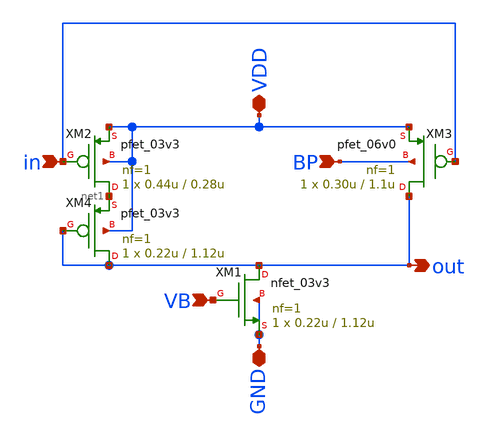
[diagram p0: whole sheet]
** sch_path: xschem_designs/STI_P.sch
**.subckt STI_P in out GND VDD BP VB
*.ipin in
*.opin out
*.iopin GND
*.iopin VDD
*.ipin BP
*.ipin VB
XM1 out VB GND GND nfet_03v3 L=1.12u W=0.22u nf=1 ad='int((nf+1)/2) * W/nf * 0.18u' as='int((nf+2)/2) * W/nf * 0.18u'
+ pd='2*int((nf+1)/2) * (W/nf + 0.18u)' ps='2*int((nf+2)/2) * (W/nf + 0.18u)' nrd='0.18u / W' nrs='0.18u / W'
+ sa=0 sb=0 sd=0 m=1 par=1
XM2 net1 in VDD VDD pfet_03v3 L=0.28u W=0.44u nf=1 ad='int((nf+1)/2) * W/nf * 0.18u' as='int((nf+2)/2) * W/nf * 0.18u'
+ pd='2*int((nf+1)/2) * (W/nf + 0.18u)' ps='2*int((nf+2)/2) * (W/nf + 0.18u)' nrd='0.18u / W' nrs='0.18u / W'
+ sa=0 sb=0 sd=0 m=1 par=1
XM3 out in VDD BP pfet_06v0 L=1.1u W=0.30u nf=1 ad='int((nf+1)/2) * W/nf * 0.18u' as='int((nf+2)/2) * W/nf * 0.18u'
+ pd='2*int((nf+1)/2) * (W/nf + 0.18u)' ps='2*int((nf+2)/2) * (W/nf + 0.18u)' nrd='0.18u / W' nrs='0.18u / W'
+ sa=0 sb=0 sd=0 m=1
XM4 out out net1 VDD pfet_03v3 L=1.12u W=0.22u nf=1 ad='int((nf+1)/2) * W/nf * 0.18u' as='int((nf+2)/2) * W/nf * 0.18u'
+ pd='2*int((nf+1)/2) * (W/nf + 0.18u)' ps='2*int((nf+2)/2) * (W/nf + 0.18u)' nrd='0.18u / W' nrs='0.18u / W'
+ sa=0 sb=0 sd=0 m=1 par=1
**.ends
.end
